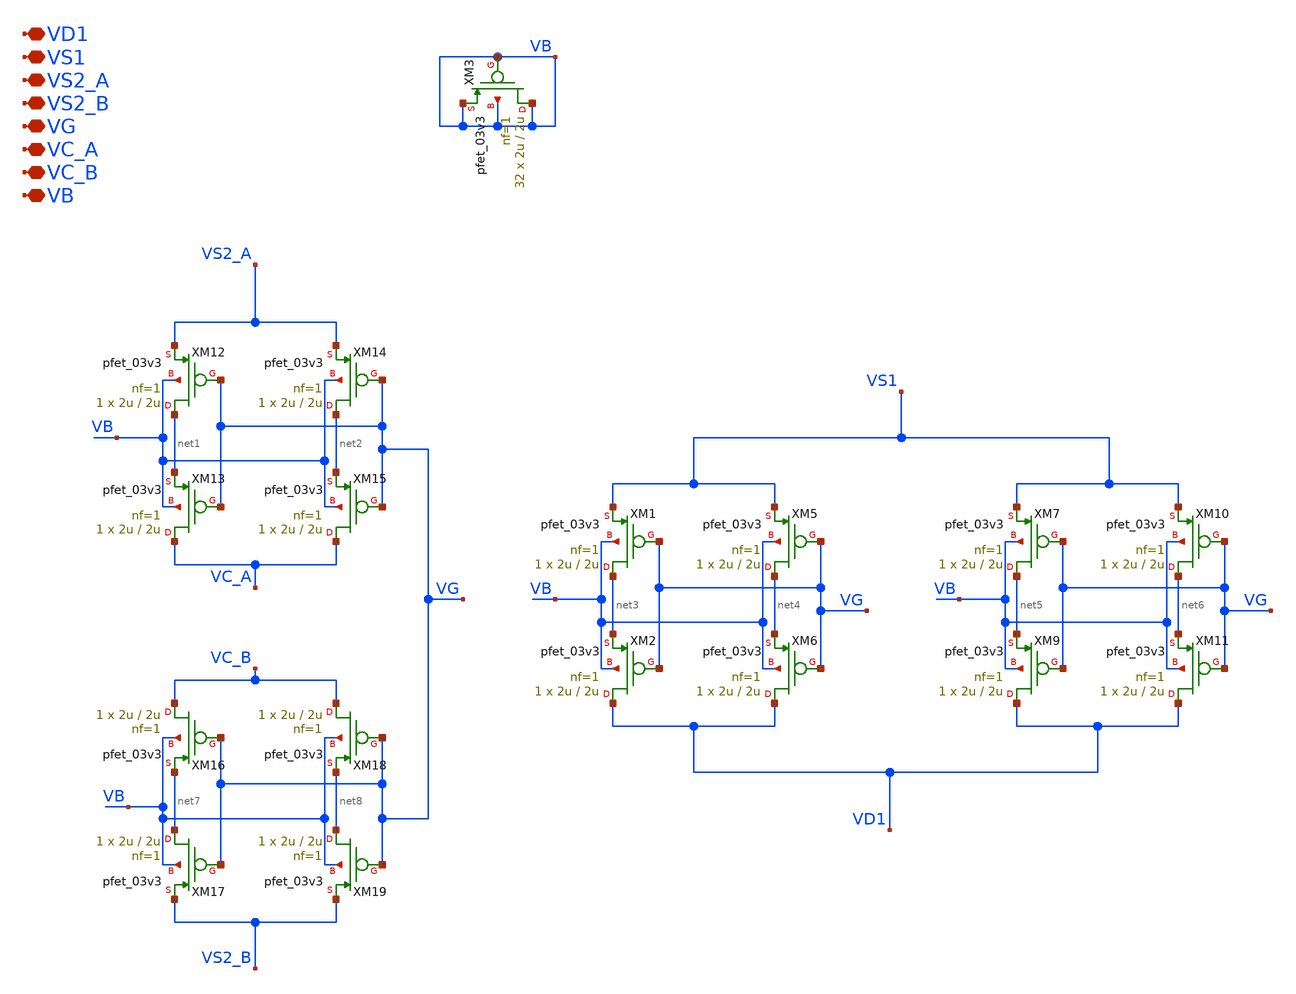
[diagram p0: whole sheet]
** sch_path: TIA/xschem/PseudoResistor/PR_pfets.sch
**.subckt PR_pfets VD1 VS1 VS2_A VS2_B VG VC_A VC_B VB
*.iopin VD1
*.iopin VS1
*.iopin VS2_A
*.iopin VS2_B
*.iopin VG
*.iopin VC_A
*.iopin VC_B
*.iopin VB
XM1 net3 VG VS1 VB pfet_03v3 L=2u W=2u nf=1 ad='int((nf+1)/2) * W/nf * 0.18u' as='int((nf+2)/2) * W/nf * 0.18u'
+ pd='2*int((nf+1)/2) * (W/nf + 0.18u)' ps='2*int((nf+2)/2) * (W/nf + 0.18u)' nrd='0.18u / W' nrs='0.18u / W'
+ sa=0 sb=0 sd=0 m=1
XM2 VD1 VG net3 VB pfet_03v3 L=2u W=2u nf=1 ad='int((nf+1)/2) * W/nf * 0.18u' as='int((nf+2)/2) * W/nf * 0.18u'
+ pd='2*int((nf+1)/2) * (W/nf + 0.18u)' ps='2*int((nf+2)/2) * (W/nf + 0.18u)' nrd='0.18u / W' nrs='0.18u / W'
+ sa=0 sb=0 sd=0 m=1
XM5 net4 VG VS1 VB pfet_03v3 L=2u W=2u nf=1 ad='int((nf+1)/2) * W/nf * 0.18u' as='int((nf+2)/2) * W/nf * 0.18u'
+ pd='2*int((nf+1)/2) * (W/nf + 0.18u)' ps='2*int((nf+2)/2) * (W/nf + 0.18u)' nrd='0.18u / W' nrs='0.18u / W'
+ sa=0 sb=0 sd=0 m=1
XM6 VD1 VG net4 VB pfet_03v3 L=2u W=2u nf=1 ad='int((nf+1)/2) * W/nf * 0.18u' as='int((nf+2)/2) * W/nf * 0.18u'
+ pd='2*int((nf+1)/2) * (W/nf + 0.18u)' ps='2*int((nf+2)/2) * (W/nf + 0.18u)' nrd='0.18u / W' nrs='0.18u / W'
+ sa=0 sb=0 sd=0 m=1
XM7 net5 VG VS1 VB pfet_03v3 L=2u W=2u nf=1 ad='int((nf+1)/2) * W/nf * 0.18u' as='int((nf+2)/2) * W/nf * 0.18u'
+ pd='2*int((nf+1)/2) * (W/nf + 0.18u)' ps='2*int((nf+2)/2) * (W/nf + 0.18u)' nrd='0.18u / W' nrs='0.18u / W'
+ sa=0 sb=0 sd=0 m=1
XM9 VD1 VG net5 VB pfet_03v3 L=2u W=2u nf=1 ad='int((nf+1)/2) * W/nf * 0.18u' as='int((nf+2)/2) * W/nf * 0.18u'
+ pd='2*int((nf+1)/2) * (W/nf + 0.18u)' ps='2*int((nf+2)/2) * (W/nf + 0.18u)' nrd='0.18u / W' nrs='0.18u / W'
+ sa=0 sb=0 sd=0 m=1
XM10 net6 VG VS1 VB pfet_03v3 L=2u W=2u nf=1 ad='int((nf+1)/2) * W/nf * 0.18u' as='int((nf+2)/2) * W/nf * 0.18u'
+ pd='2*int((nf+1)/2) * (W/nf + 0.18u)' ps='2*int((nf+2)/2) * (W/nf + 0.18u)' nrd='0.18u / W' nrs='0.18u / W'
+ sa=0 sb=0 sd=0 m=1
XM11 VD1 VG net6 VB pfet_03v3 L=2u W=2u nf=1 ad='int((nf+1)/2) * W/nf * 0.18u' as='int((nf+2)/2) * W/nf * 0.18u'
+ pd='2*int((nf+1)/2) * (W/nf + 0.18u)' ps='2*int((nf+2)/2) * (W/nf + 0.18u)' nrd='0.18u / W' nrs='0.18u / W'
+ sa=0 sb=0 sd=0 m=1
XM12 net1 VG VS2_A VB pfet_03v3 L=2u W=2u nf=1 ad='int((nf+1)/2) * W/nf * 0.18u' as='int((nf+2)/2) * W/nf * 0.18u'
+ pd='2*int((nf+1)/2) * (W/nf + 0.18u)' ps='2*int((nf+2)/2) * (W/nf + 0.18u)' nrd='0.18u / W' nrs='0.18u / W'
+ sa=0 sb=0 sd=0 m=1
XM13 VC_A VG net1 VB pfet_03v3 L=2u W=2u nf=1 ad='int((nf+1)/2) * W/nf * 0.18u' as='int((nf+2)/2) * W/nf * 0.18u'
+ pd='2*int((nf+1)/2) * (W/nf + 0.18u)' ps='2*int((nf+2)/2) * (W/nf + 0.18u)' nrd='0.18u / W' nrs='0.18u / W'
+ sa=0 sb=0 sd=0 m=1
XM14 net2 VG VS2_A VB pfet_03v3 L=2u W=2u nf=1 ad='int((nf+1)/2) * W/nf * 0.18u' as='int((nf+2)/2) * W/nf * 0.18u'
+ pd='2*int((nf+1)/2) * (W/nf + 0.18u)' ps='2*int((nf+2)/2) * (W/nf + 0.18u)' nrd='0.18u / W' nrs='0.18u / W'
+ sa=0 sb=0 sd=0 m=1
XM15 VC_A VG net2 VB pfet_03v3 L=2u W=2u nf=1 ad='int((nf+1)/2) * W/nf * 0.18u' as='int((nf+2)/2) * W/nf * 0.18u'
+ pd='2*int((nf+1)/2) * (W/nf + 0.18u)' ps='2*int((nf+2)/2) * (W/nf + 0.18u)' nrd='0.18u / W' nrs='0.18u / W'
+ sa=0 sb=0 sd=0 m=1
XM16 VC_B VG net7 VB pfet_03v3 L=2u W=2u nf=1 ad='int((nf+1)/2) * W/nf * 0.18u' as='int((nf+2)/2) * W/nf * 0.18u'
+ pd='2*int((nf+1)/2) * (W/nf + 0.18u)' ps='2*int((nf+2)/2) * (W/nf + 0.18u)' nrd='0.18u / W' nrs='0.18u / W'
+ sa=0 sb=0 sd=0 m=1
XM17 net7 VG VS2_B VB pfet_03v3 L=2u W=2u nf=1 ad='int((nf+1)/2) * W/nf * 0.18u' as='int((nf+2)/2) * W/nf * 0.18u'
+ pd='2*int((nf+1)/2) * (W/nf + 0.18u)' ps='2*int((nf+2)/2) * (W/nf + 0.18u)' nrd='0.18u / W' nrs='0.18u / W'
+ sa=0 sb=0 sd=0 m=1
XM18 VC_B VG net8 VB pfet_03v3 L=2u W=2u nf=1 ad='int((nf+1)/2) * W/nf * 0.18u' as='int((nf+2)/2) * W/nf * 0.18u'
+ pd='2*int((nf+1)/2) * (W/nf + 0.18u)' ps='2*int((nf+2)/2) * (W/nf + 0.18u)' nrd='0.18u / W' nrs='0.18u / W'
+ sa=0 sb=0 sd=0 m=1
XM19 net8 VG VS2_B VB pfet_03v3 L=2u W=2u nf=1 ad='int((nf+1)/2) * W/nf * 0.18u' as='int((nf+2)/2) * W/nf * 0.18u'
+ pd='2*int((nf+1)/2) * (W/nf + 0.18u)' ps='2*int((nf+2)/2) * (W/nf + 0.18u)' nrd='0.18u / W' nrs='0.18u / W'
+ sa=0 sb=0 sd=0 m=1
XM3 VB VB VB VB pfet_03v3 L=2u W=2u nf=1 ad='int((nf+1)/2) * W/nf * 0.18u' as='int((nf+2)/2) * W/nf * 0.18u'
+ pd='2*int((nf+1)/2) * (W/nf + 0.18u)' ps='2*int((nf+2)/2) * (W/nf + 0.18u)' nrd='0.18u / W' nrs='0.18u / W'
+ sa=0 sb=0 sd=0 m=32
**.ends
.end
